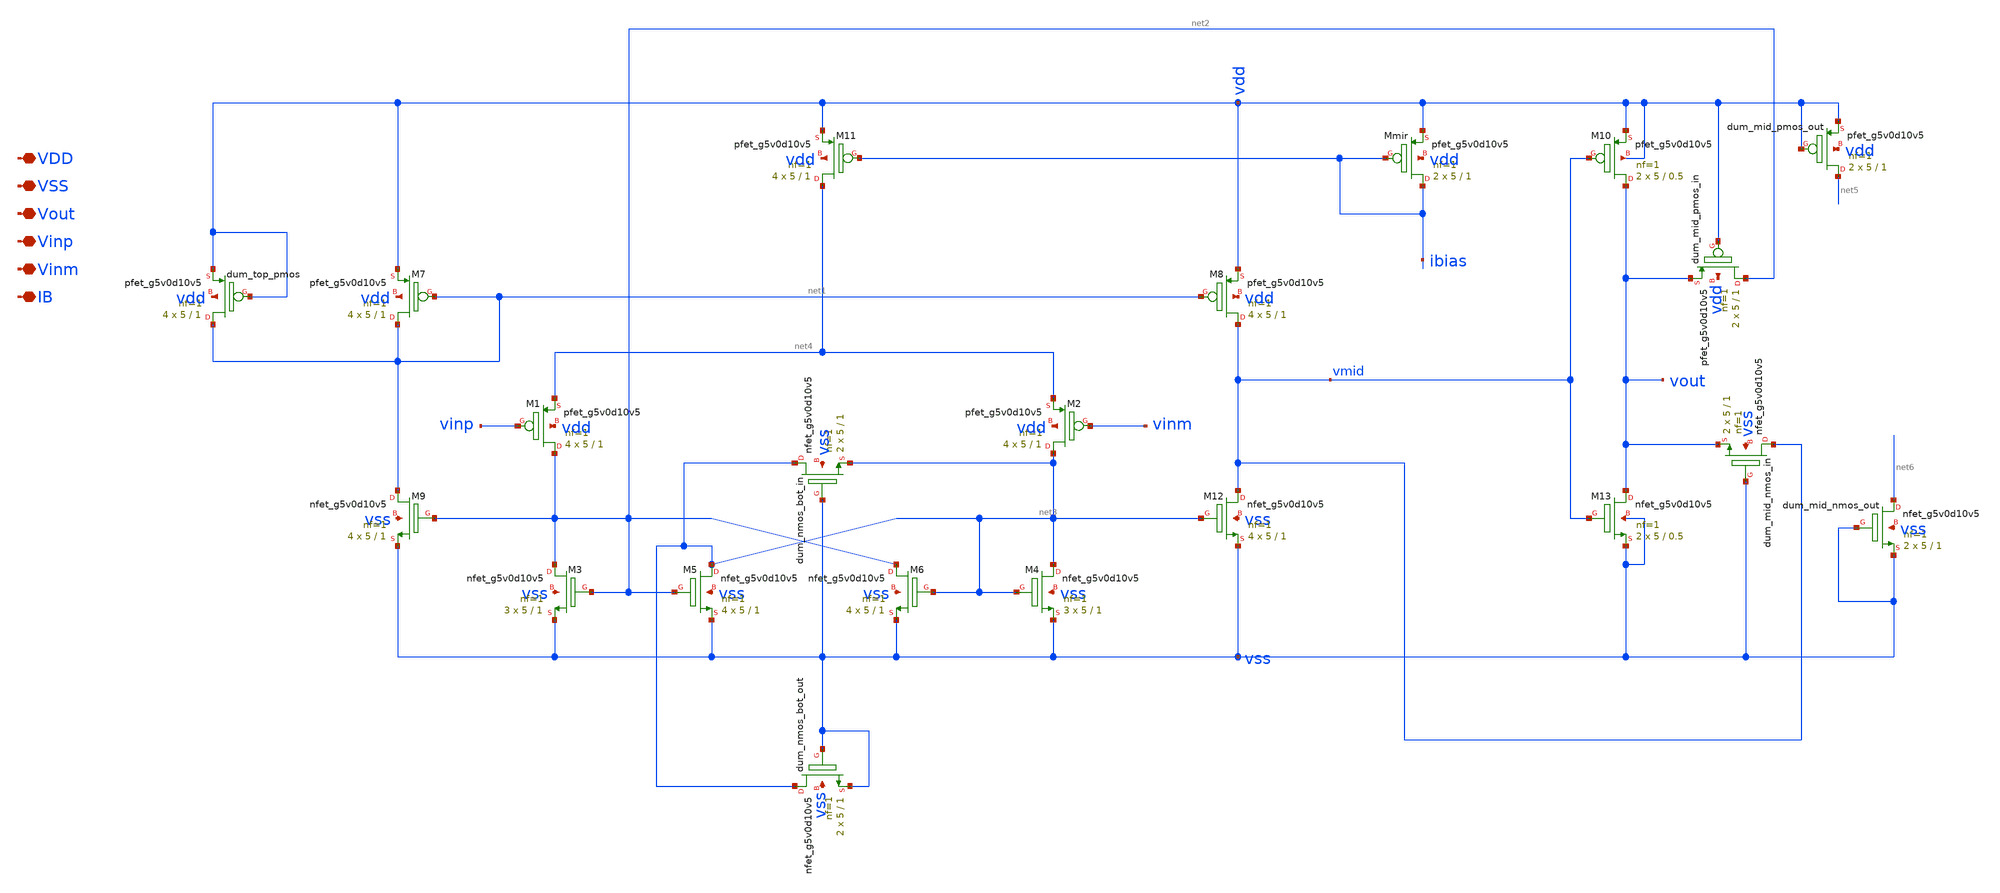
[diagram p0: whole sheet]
** sch_path: design/comparator/comparator_w_obuff_4LVS.sch
**.subckt comparator_w_obuff_4LVS VDD VSS Vout Vinp Vinm IB
*.iopin VDD
*.iopin VSS
*.iopin Vout
*.iopin Vinp
*.iopin Vinm
*.iopin IB
XM11 net4 ibias vdd vdd sky130_fd_pr__pfet_g5v0d10v5 L=1 W=5 nf=1 ad='int((nf+1)/2) * W/nf * 0.29' as='int((nf+2)/2) * W/nf * 0.29'
+ pd='2*int((nf+1)/2) * (W/nf + 0.29)' ps='2*int((nf+2)/2) * (W/nf + 0.29)' nrd='0.29 / W' nrs='0.29 / W'
+ sa=0 sb=0 sd=0 mult=4 m=4
XM8 vmid net1 vdd vdd sky130_fd_pr__pfet_g5v0d10v5 L=1 W=5 nf=1 ad='int((nf+1)/2) * W/nf * 0.29' as='int((nf+2)/2) * W/nf * 0.29'
+ pd='2*int((nf+1)/2) * (W/nf + 0.29)' ps='2*int((nf+2)/2) * (W/nf + 0.29)' nrd='0.29 / W' nrs='0.29 / W'
+ sa=0 sb=0 sd=0 mult=4 m=4
XM7 net1 net1 vdd vdd sky130_fd_pr__pfet_g5v0d10v5 L=1 W=5 nf=1 ad='int((nf+1)/2) * W/nf * 0.29' as='int((nf+2)/2) * W/nf * 0.29'
+ pd='2*int((nf+1)/2) * (W/nf + 0.29)' ps='2*int((nf+2)/2) * (W/nf + 0.29)' nrd='0.29 / W' nrs='0.29 / W'
+ sa=0 sb=0 sd=0 mult=4 m=4
XM2 net3 vinm net4 vdd sky130_fd_pr__pfet_g5v0d10v5 L=1 W=5 nf=1 ad='int((nf+1)/2) * W/nf * 0.29' as='int((nf+2)/2) * W/nf * 0.29'
+ pd='2*int((nf+1)/2) * (W/nf + 0.29)' ps='2*int((nf+2)/2) * (W/nf + 0.29)' nrd='0.29 / W' nrs='0.29 / W'
+ sa=0 sb=0 sd=0 mult=4 m=4
XM1 net2 vinp net4 vdd sky130_fd_pr__pfet_g5v0d10v5 L=1 W=5 nf=1 ad='int((nf+1)/2) * W/nf * 0.29' as='int((nf+2)/2) * W/nf * 0.29'
+ pd='2*int((nf+1)/2) * (W/nf + 0.29)' ps='2*int((nf+2)/2) * (W/nf + 0.29)' nrd='0.29 / W' nrs='0.29 / W'
+ sa=0 sb=0 sd=0 mult=4 m=4
XMmir ibias ibias vdd vdd sky130_fd_pr__pfet_g5v0d10v5 L=1 W=5 nf=1 ad='int((nf+1)/2) * W/nf * 0.29'
+ as='int((nf+2)/2) * W/nf * 0.29' pd='2*int((nf+1)/2) * (W/nf + 0.29)' ps='2*int((nf+2)/2) * (W/nf + 0.29)'
+ nrd='0.29 / W' nrs='0.29 / W' sa=0 sb=0 sd=0 mult=2 m=2
XM12 vmid net3 vss vss sky130_fd_pr__nfet_g5v0d10v5 L=1 W=5 nf=1 ad='int((nf+1)/2) * W/nf * 0.29' as='int((nf+2)/2) * W/nf * 0.29'
+ pd='2*int((nf+1)/2) * (W/nf + 0.29)' ps='2*int((nf+2)/2) * (W/nf + 0.29)' nrd='0.29 / W' nrs='0.29 / W'
+ sa=0 sb=0 sd=0 mult=4 m=4
XM4 net3 net3 vss vss sky130_fd_pr__nfet_g5v0d10v5 L=1 W=5 nf=1 ad='int((nf+1)/2) * W/nf * 0.29' as='int((nf+2)/2) * W/nf * 0.29'
+ pd='2*int((nf+1)/2) * (W/nf + 0.29)' ps='2*int((nf+2)/2) * (W/nf + 0.29)' nrd='0.29 / W' nrs='0.29 / W'
+ sa=0 sb=0 sd=0 mult=3 m=3
XM6 net2 net3 vss vss sky130_fd_pr__nfet_g5v0d10v5 L=1 W=5 nf=1 ad='int((nf+1)/2) * W/nf * 0.29' as='int((nf+2)/2) * W/nf * 0.29'
+ pd='2*int((nf+1)/2) * (W/nf + 0.29)' ps='2*int((nf+2)/2) * (W/nf + 0.29)' nrd='0.29 / W' nrs='0.29 / W'
+ sa=0 sb=0 sd=0 mult=4 m=4
XM5 net3 net2 vss vss sky130_fd_pr__nfet_g5v0d10v5 L=1 W=5 nf=1 ad='int((nf+1)/2) * W/nf * 0.29' as='int((nf+2)/2) * W/nf * 0.29'
+ pd='2*int((nf+1)/2) * (W/nf + 0.29)' ps='2*int((nf+2)/2) * (W/nf + 0.29)' nrd='0.29 / W' nrs='0.29 / W'
+ sa=0 sb=0 sd=0 mult=4 m=4
XM3 net2 net2 vss vss sky130_fd_pr__nfet_g5v0d10v5 L=1 W=5 nf=1 ad='int((nf+1)/2) * W/nf * 0.29' as='int((nf+2)/2) * W/nf * 0.29'
+ pd='2*int((nf+1)/2) * (W/nf + 0.29)' ps='2*int((nf+2)/2) * (W/nf + 0.29)' nrd='0.29 / W' nrs='0.29 / W'
+ sa=0 sb=0 sd=0 mult=3 m=3
XM9 net1 net2 vss vss sky130_fd_pr__nfet_g5v0d10v5 L=1 W=5 nf=1 ad='int((nf+1)/2) * W/nf * 0.29' as='int((nf+2)/2) * W/nf * 0.29'
+ pd='2*int((nf+1)/2) * (W/nf + 0.29)' ps='2*int((nf+2)/2) * (W/nf + 0.29)' nrd='0.29 / W' nrs='0.29 / W'
+ sa=0 sb=0 sd=0 mult=4 m=4
XM10 vout vmid vdd vdd sky130_fd_pr__pfet_g5v0d10v5 L=0.5 W=5 nf=1 ad='int((nf+1)/2) * W/nf * 0.29' as='int((nf+2)/2) * W/nf * 0.29'
+ pd='2*int((nf+1)/2) * (W/nf + 0.29)' ps='2*int((nf+2)/2) * (W/nf + 0.29)' nrd='0.29 / W' nrs='0.29 / W'
+ sa=0 sb=0 sd=0 mult=2 m=2
XM13 vout vmid vss vss sky130_fd_pr__nfet_g5v0d10v5 L=0.5 W=5 nf=1 ad='int((nf+1)/2) * W/nf * 0.29' as='int((nf+2)/2) * W/nf * 0.29'
+ pd='2*int((nf+1)/2) * (W/nf + 0.29)' ps='2*int((nf+2)/2) * (W/nf + 0.29)' nrd='0.29 / W' nrs='0.29 / W'
+ sa=0 sb=0 sd=0 mult=2 m=2
Xdum_top_pmos net1 vdd vdd vdd sky130_fd_pr__pfet_g5v0d10v5 L=1 W=5 nf=1 ad='int((nf+1)/2) * W/nf * 0.29'
+ as='int((nf+2)/2) * W/nf * 0.29' pd='2*int((nf+1)/2) * (W/nf + 0.29)' ps='2*int((nf+2)/2) * (W/nf + 0.29)'
+ nrd='0.29 / W' nrs='0.29 / W' sa=0 sb=0 sd=0 mult=4 m=4
Xdum_mid_pmos_out net5 vdd vdd vdd sky130_fd_pr__pfet_g5v0d10v5 L=1 W=5 nf=1 ad='int((nf+1)/2) * W/nf * 0.29'
+ as='int((nf+2)/2) * W/nf * 0.29' pd='2*int((nf+1)/2) * (W/nf + 0.29)' ps='2*int((nf+2)/2) * (W/nf + 0.29)'
+ nrd='0.29 / W' nrs='0.29 / W' sa=0 sb=0 sd=0 mult=2 m=2
Xdum_mid_pmos_in net2 vdd vout vdd sky130_fd_pr__pfet_g5v0d10v5 L=1 W=5 nf=1 ad='int((nf+1)/2) * W/nf * 0.29'
+ as='int((nf+2)/2) * W/nf * 0.29' pd='2*int((nf+1)/2) * (W/nf + 0.29)' ps='2*int((nf+2)/2) * (W/nf + 0.29)'
+ nrd='0.29 / W' nrs='0.29 / W' sa=0 sb=0 sd=0 mult=2 m=2
Xdum_mid_nmos_out net6 vss vss vss sky130_fd_pr__nfet_g5v0d10v5 L=1 W=5 nf=1 ad='int((nf+1)/2) * W/nf * 0.29'
+ as='int((nf+2)/2) * W/nf * 0.29' pd='2*int((nf+1)/2) * (W/nf + 0.29)' ps='2*int((nf+2)/2) * (W/nf + 0.29)'
+ nrd='0.29 / W' nrs='0.29 / W' sa=0 sb=0 sd=0 mult=2 m=2
Xdum_mid_nmos_in vmid vss vout vss sky130_fd_pr__nfet_g5v0d10v5 L=1 W=5 nf=1 ad='int((nf+1)/2) * W/nf * 0.29'
+ as='int((nf+2)/2) * W/nf * 0.29' pd='2*int((nf+1)/2) * (W/nf + 0.29)' ps='2*int((nf+2)/2) * (W/nf + 0.29)'
+ nrd='0.29 / W' nrs='0.29 / W' sa=0 sb=0 sd=0 mult=2 m=2
Xdum_nmos_bot_in net3 vss net3 vss sky130_fd_pr__nfet_g5v0d10v5 L=1 W=5 nf=1 ad='int((nf+1)/2) * W/nf * 0.29'
+ as='int((nf+2)/2) * W/nf * 0.29' pd='2*int((nf+1)/2) * (W/nf + 0.29)' ps='2*int((nf+2)/2) * (W/nf + 0.29)'
+ nrd='0.29 / W' nrs='0.29 / W' sa=0 sb=0 sd=0 mult=2 m=2
Xdum_nmos_bot_out net3 vss vss vss sky130_fd_pr__nfet_g5v0d10v5 L=1 W=5 nf=1 ad='int((nf+1)/2) * W/nf * 0.29'
+ as='int((nf+2)/2) * W/nf * 0.29' pd='2*int((nf+1)/2) * (W/nf + 0.29)' ps='2*int((nf+2)/2) * (W/nf + 0.29)'
+ nrd='0.29 / W' nrs='0.29 / W' sa=0 sb=0 sd=0 mult=2 m=2
**.ends
.end
